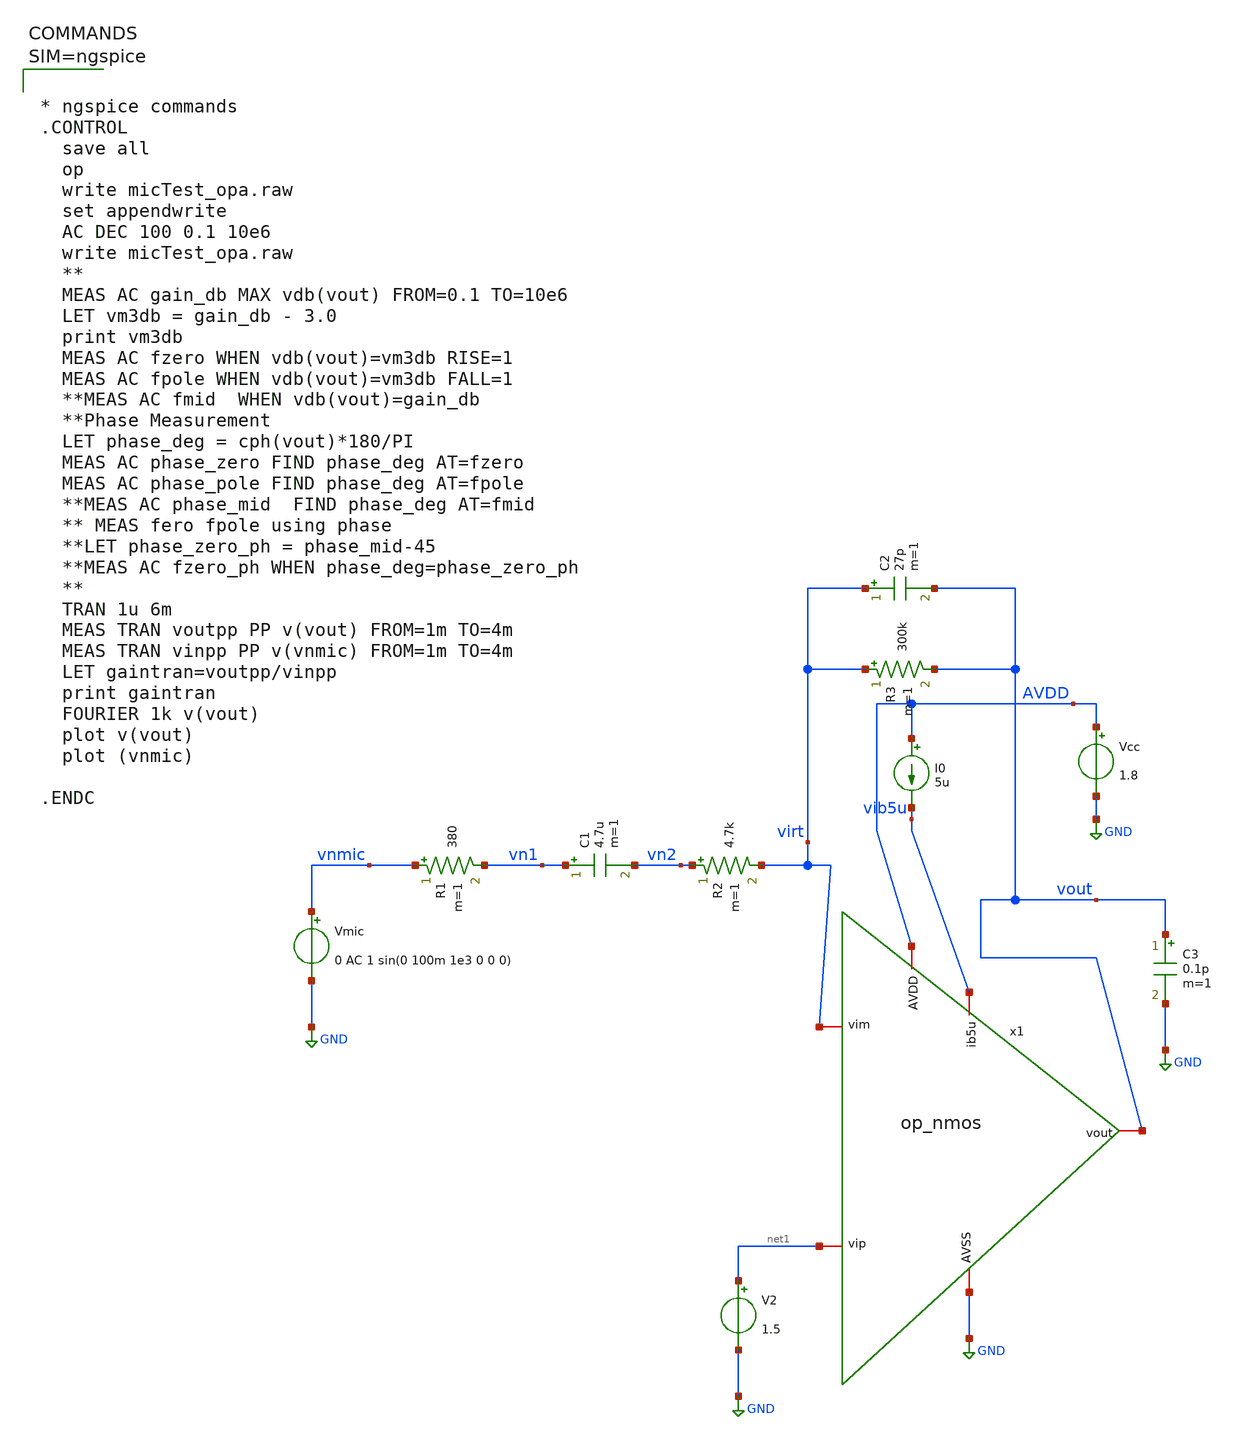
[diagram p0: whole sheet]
** sch_path: xschem/untitled-11.sch
**.subckt untitled-11
Vmic vnmic GND 0 AC 1 sin(0 100m 1e3 0 0 0)
R1 vnmic vn1 380 m=1
C1 vn1 vn2 4.7u m=1
R2 vn2 virt 4.7k m=1
R3 virt vout 300k m=1
C2 virt vout 27p m=1
V2 net1 GND 1.5
C3 vout GND 0.1p m=1
Vcc AVDD GND 1.8
I0 AVDD vib5u 5u
x1 AVDD vout virt net1 vib5u GND op_nmos
**** begin user architecture code



* ngspice commands
.CONTROL
  save all
  op
  write micTest_opa.raw
  set appendwrite
  AC DEC 100 0.1 10e6
  write micTest_opa.raw
  **
  MEAS AC gain_db MAX vdb(vout) FROM=0.1 TO=10e6
  LET vm3db = gain_db - 3.0
  print vm3db
  MEAS AC fzero WHEN vdb(vout)=vm3db RISE=1
  MEAS AC fpole WHEN vdb(vout)=vm3db FALL=1
  **MEAS AC fmid  WHEN vdb(vout)=gain_db
  **Phase Measurement
  LET phase_deg = cph(vout)*180/PI
  MEAS AC phase_zero FIND phase_deg AT=fzero
  MEAS AC phase_pole FIND phase_deg AT=fpole
  **MEAS AC phase_mid  FIND phase_deg AT=fmid
  ** MEAS fero fpole using phase
  **LET phase_zero_ph = phase_mid-45
  **MEAS AC fzero_ph WHEN phase_deg=phase_zero_ph
  **
  TRAN 1u 6m
  MEAS TRAN voutpp PP v(vout) FROM=1m TO=4m
  MEAS TRAN vinpp PP v(vnmic) FROM=1m TO=4m
  LET gaintran=voutpp/vinpp
  print gaintran
  FOURIER 1k v(vout)
  plot v(vout)
  plot (vnmic)

.ENDC




** opencircuitdesign pdks install
.lib $::SKYWATER_MODELS/sky130.lib.spice tt

**** end user architecture code
**.ends

* expanding   symbol:  op_nmos.sym # of pins=6
** sym_path: xschem/op_nmos.sym
** sch_path: xschem/op_nmos.sch
.subckt op_nmos AVDD vout vim vip ib5u AVSS
*.iopin ib5u
*.iopin AVSS
*.iopin vim
*.iopin vip
*.iopin AVDD
*.iopin vout
XM1 ib5u ib5u AVSS AVSS sky130_fd_pr__nfet_01v8 L=1 W=5 nf=1 ad='int((1 + 1)/2) * 5 / 1 * 0.29' as='int((1 + 2)/2) * 5 / 1 * 0.29'
+ pd='2*int((1 + 1)/2) * (5 / 1 + 0.29)' ps='2*int((1 + 2)/2) * (5 / 1 + 0.29)' nrd='0.29 / 5 ' nrs='0.29 / 5 '
+ sa=0 sb=0 sd=0 mult=1 m=1
XMtail net1 ib5u AVSS AVSS sky130_fd_pr__nfet_01v8 L=1 W=5 nf=1 ad='int((1 + 1)/2) * 5 / 1 * 0.29' as='int((1 + 2)/2) * 5 / 1 * 0.29'
+ pd='2*int((1 + 1)/2) * (5 / 1 + 0.29)' ps='2*int((1 + 2)/2) * (5 / 1 + 0.29)' nrd='0.29 / 5 ' nrs='0.29 / 5 '
+ sa=0 sb=0 sd=0 mult=1 m=1
XMip vom vip net1 net1 sky130_fd_pr__nfet_01v8_lvt L=2 W=5 nf=1 ad='int((1 + 1)/2) * 5 / 1 * 0.29' as='int((1 + 2)/2) * 5 / 1 * 0.29'
+ pd='2*int((1 + 1)/2) * (5 / 1 + 0.29)' ps='2*int((1 + 2)/2) * (5 / 1 + 0.29)' nrd='0.29 / 5 ' nrs='0.29 / 5 '
+ sa=0 sb=0 sd=0 mult=4 m=4
XMim vout vim net1 net1 sky130_fd_pr__nfet_01v8_lvt L=2 W=5 nf=1 ad='int((1 + 1)/2) * 5 / 1 * 0.29' as='int((1 + 2)/2) * 5 / 1 * 0.29'
+ pd='2*int((1 + 1)/2) * (5 / 1 + 0.29)' ps='2*int((1 + 2)/2) * (5 / 1 + 0.29)' nrd='0.29 / 5 ' nrs='0.29 / 5 '
+ sa=0 sb=0 sd=0 mult=4 m=4
XMpcmp vom vom AVDD AVDD sky130_fd_pr__pfet_01v8_lvt L=2 W=5 nf=1 ad='int((1 + 1)/2) * 5 / 1 * 0.29'
+ as='int((1 + 2)/2) * 5 / 1 * 0.29' pd='2*int((1 + 1)/2) * (5 / 1 + 0.29)' ps='2*int((1 + 2)/2) * (5 / 1 + 0.29)'
+ nrd='0.29 / 5 ' nrs='0.29 / 5 ' sa=0 sb=0 sd=0 mult=2 m=2
XMpcmm vout vom AVDD AVDD sky130_fd_pr__pfet_01v8_lvt L=2 W=5 nf=1 ad='int((1 + 1)/2) * 5 / 1 * 0.29'
+ as='int((1 + 2)/2) * 5 / 1 * 0.29' pd='2*int((1 + 1)/2) * (5 / 1 + 0.29)' ps='2*int((1 + 2)/2) * (5 / 1 + 0.29)'
+ nrd='0.29 / 5 ' nrs='0.29 / 5 ' sa=0 sb=0 sd=0 mult=2 m=2
.ends

.GLOBAL GND
.end
